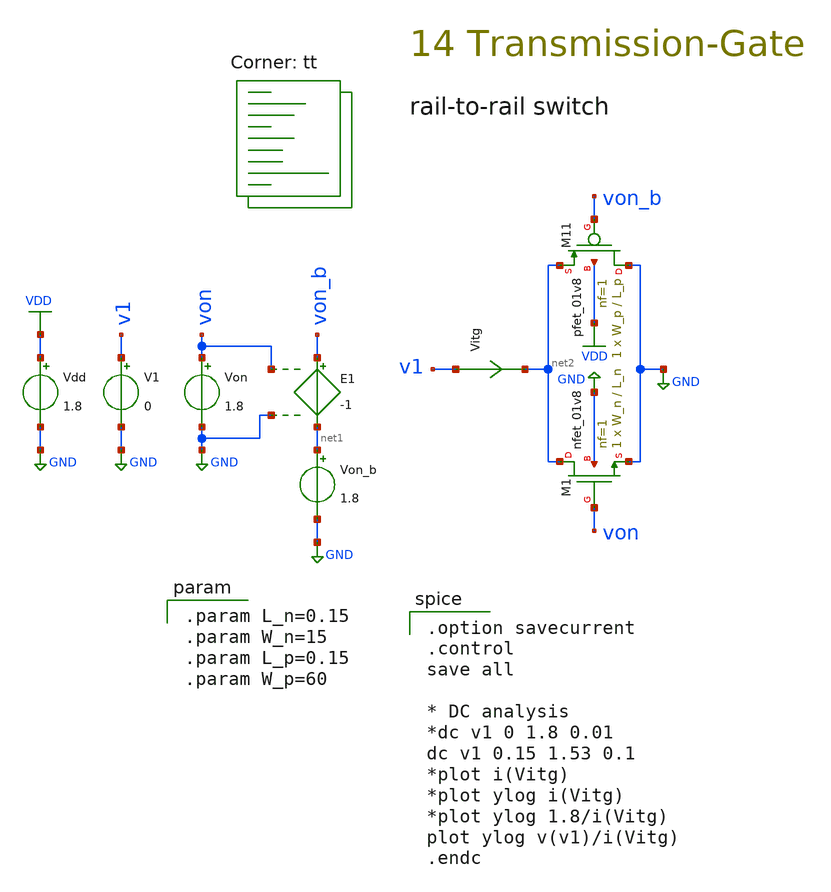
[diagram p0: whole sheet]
** sch_path: tseng_workspace/transmission_gate/schematic/spice/tg_dc_tb.sch
**.subckt tg_dc_tb
XM1 net2 von GND GND sky130_fd_pr__nfet_01v8 L=L_n W=W_n nf=1 ad='int((1 + 1)/2) * W_n / 1 * 0.29' as='int((1 + 2)/2) * W_n / 1 * 0.29'
+ pd='2*int((1 + 1)/2) * (W_n / 1 + 0.29)' ps='2*int((1 + 2)/2) * (W_n / 1 + 0.29)' nrd='0.29 / W_n ' nrs='0.29 / W_n '
+ sa=0 sb=0 sd=0 mult=1 m=1
V1 v1 GND 0
Von von GND 1.8
E1 von_b net1 von GND -1
Von_b net1 GND 1.8
XM11 GND von_b net2 VDD sky130_fd_pr__pfet_01v8 L=L_p W=W_p nf=1 ad='int((nf+1)/2) * W/nf * 0.29' as='int((nf+2)/2) * W/nf * 0.29'
+ pd='2*int((nf+1)/2) * (W/nf + 0.29)' ps='2*int((nf+2)/2) * (W/nf + 0.29)' nrd='0.29 / W' nrs='0.29 / W'
+ sa=0 sb=0 sd=0 mult=1 m=1
Vdd VDD GND 1.8
Vitg v1 net2 0
.save i(vitg)
**** begin user architecture code
.lib $::SKYWATER_MODELS/sky130.lib.spice tt

.option savecurrent
.control
save all

* DC analysis
*dc v1 0 1.8 0.01
dc v1 0.15 1.53 0.1
*plot i(Vitg)
*plot ylog i(Vitg)
*plot ylog 1.8/i(Vitg)
plot ylog v(v1)/i(Vitg)
.endc


.param L_n=0.15
.param W_n=15
.param L_p=0.15
.param W_p=60

**** end user architecture code
**.ends
.GLOBAL GND
.GLOBAL VDD
.end
